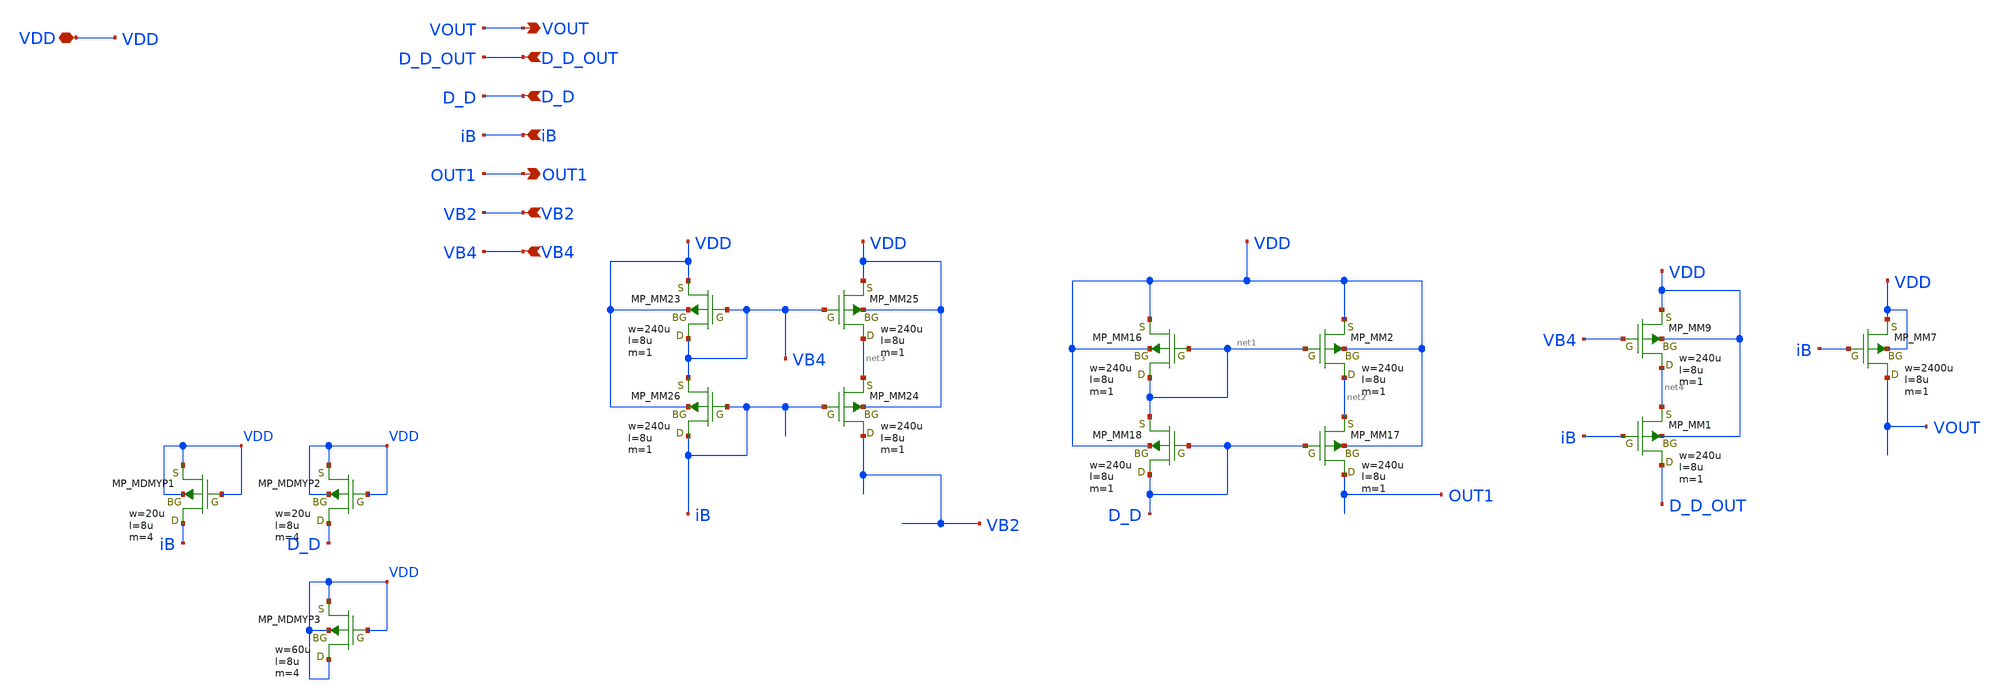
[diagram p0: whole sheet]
** sch_path: member_project/AM_Radio/noritsuna/xschem/OPAMP_PMOS_single.sch
**.subckt OPAMP_PMOS_single VDD OUT1 iB D_D VB2 VB4 D_D_OUT VOUT
*.iopin VDD
*.opin OUT1
*.ipin iB
*.ipin D_D
*.ipin VB2
*.ipin VB4
*.ipin D_D_OUT
*.opin VOUT
MM2 net2 net1 VDD VDD PMOS w=240u l=8u as=0 ad=0 ps=0 pd=0 nrd=0 nrs=0 m=1
MM16 net1 net1 VDD VDD PMOS w=240u l=8u as=0 ad=0 ps=0 pd=0 nrd=0 nrs=0 m=1
MM17 OUT1 D_D net2 VDD PMOS w=240u l=8u as=0 ad=0 ps=0 pd=0 nrd=0 nrs=0 m=1
MM18 D_D D_D net1 VDD PMOS w=240u l=8u as=0 ad=0 ps=0 pd=0 nrd=0 nrs=0 m=1
MM23 VB4 VB4 VDD VDD PMOS w=240u l=8u as=0 ad=0 ps=0 pd=0 nrd=0 nrs=0 m=1
MM24 VB2 iB net3 VDD PMOS w=240u l=8u as=0 ad=0 ps=0 pd=0 nrd=0 nrs=0 m=1
MM25 net3 VB4 VDD VDD PMOS w=240u l=8u as=0 ad=0 ps=0 pd=0 nrd=0 nrs=0 m=1
MM26 iB iB VB4 VDD PMOS w=240u l=8u as=0 ad=0 ps=0 pd=0 nrd=0 nrs=0 m=1
MM1 D_D_OUT iB net4 VDD PMOS w=240u l=8u as=0 ad=0 ps=0 pd=0 nrd=0 nrs=0 m=1
MM9 net4 VB4 VDD VDD PMOS w=240u l=8u as=0 ad=0 ps=0 pd=0 nrd=0 nrs=0 m=1
MM7 VOUT iB VDD VDD PMOS w=2400u l=8u as=0 ad=0 ps=0 pd=0 nrd=0 nrs=0 m=1
XMDMYP1 iB VDD VDD VDD PMOS w=20u l=8u as=0 ad=0 ps=0 pd=0 nrd=0 nrs=0 m=4
XMDMYP2 D_D VDD VDD VDD PMOS w=20u l=8u as=0 ad=0 ps=0 pd=0 nrd=0 nrs=0 m=4
XMDMYP3 VDD VDD VDD VDD PMOS w=60u l=8u as=0 ad=0 ps=0 pd=0 nrd=0 nrs=0 m=4
**.ends
.end
